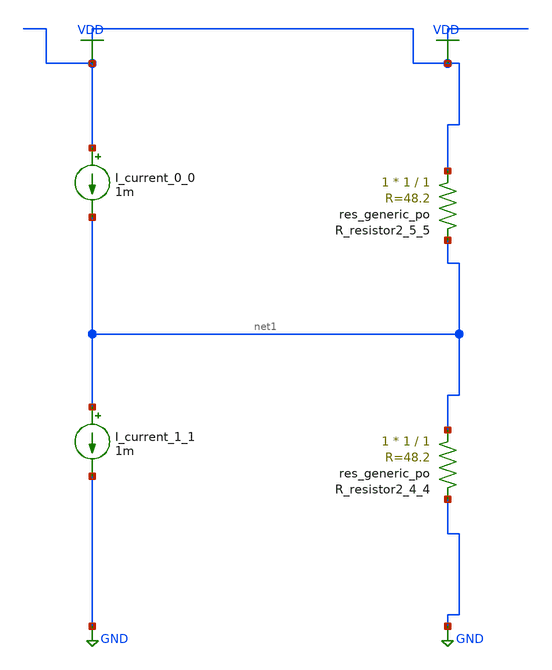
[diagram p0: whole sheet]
** sch_path: schematics/AMSNet/659.sch
**.subckt 659
I_current_0_0 VDD net1 1m
I_current_1_1 net1 GND 1m
XR_resistor2_4_4 net1 GND sky130_fd_pr__res_generic_po W=1 L=1 m=1
XR_resistor2_5_5 VDD net1 sky130_fd_pr__res_generic_po W=1 L=1 m=1
**.ends
.GLOBAL GND
.GLOBAL VDD
.end
